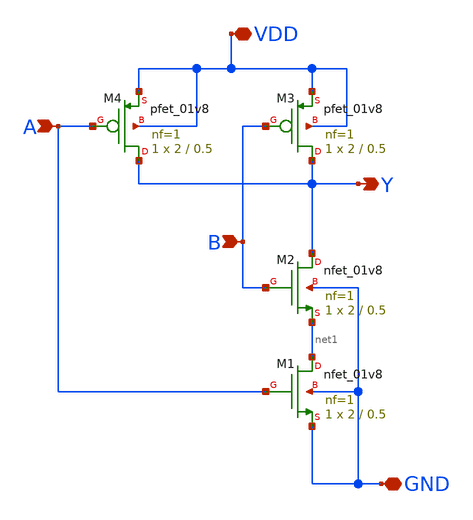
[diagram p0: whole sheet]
** sch_path: NAND/NAND.sch
**.subckt NAND A Y VDD GND B
*.ipin A
*.opin Y
*.iopin VDD
*.iopin GND
*.ipin B
XM4 Y A VDD VDD sky130_fd_pr__pfet_01v8 L=0.5 W=2 nf=1 ad='int((nf+1)/2) * W/nf * 0.29' as='int((nf+2)/2) * W/nf * 0.29'
+ pd='2*int((nf+1)/2) * (W/nf + 0.29)' ps='2*int((nf+2)/2) * (W/nf + 0.29)' nrd='0.29 / W' nrs='0.29 / W'
+ sa=0 sb=0 sd=0 mult=1 m=1
XM3 Y B VDD VDD sky130_fd_pr__pfet_01v8 L=0.5 W=2 nf=1 ad='int((nf+1)/2) * W/nf * 0.29' as='int((nf+2)/2) * W/nf * 0.29'
+ pd='2*int((nf+1)/2) * (W/nf + 0.29)' ps='2*int((nf+2)/2) * (W/nf + 0.29)' nrd='0.29 / W' nrs='0.29 / W'
+ sa=0 sb=0 sd=0 mult=1 m=1
XM2 Y B net1 GND sky130_fd_pr__nfet_01v8 L=0.5 W=2 nf=1 ad='int((nf+1)/2) * W/nf * 0.29' as='int((nf+2)/2) * W/nf * 0.29'
+ pd='2*int((nf+1)/2) * (W/nf + 0.29)' ps='2*int((nf+2)/2) * (W/nf + 0.29)' nrd='0.29 / W' nrs='0.29 / W'
+ sa=0 sb=0 sd=0 mult=1 m=1
XM1 net1 A GND GND sky130_fd_pr__nfet_01v8 L=0.5 W=2 nf=1 ad='int((nf+1)/2) * W/nf * 0.29' as='int((nf+2)/2) * W/nf * 0.29'
+ pd='2*int((nf+1)/2) * (W/nf + 0.29)' ps='2*int((nf+2)/2) * (W/nf + 0.29)' nrd='0.29 / W' nrs='0.29 / W'
+ sa=0 sb=0 sd=0 mult=1 m=1
**.ends
.end
